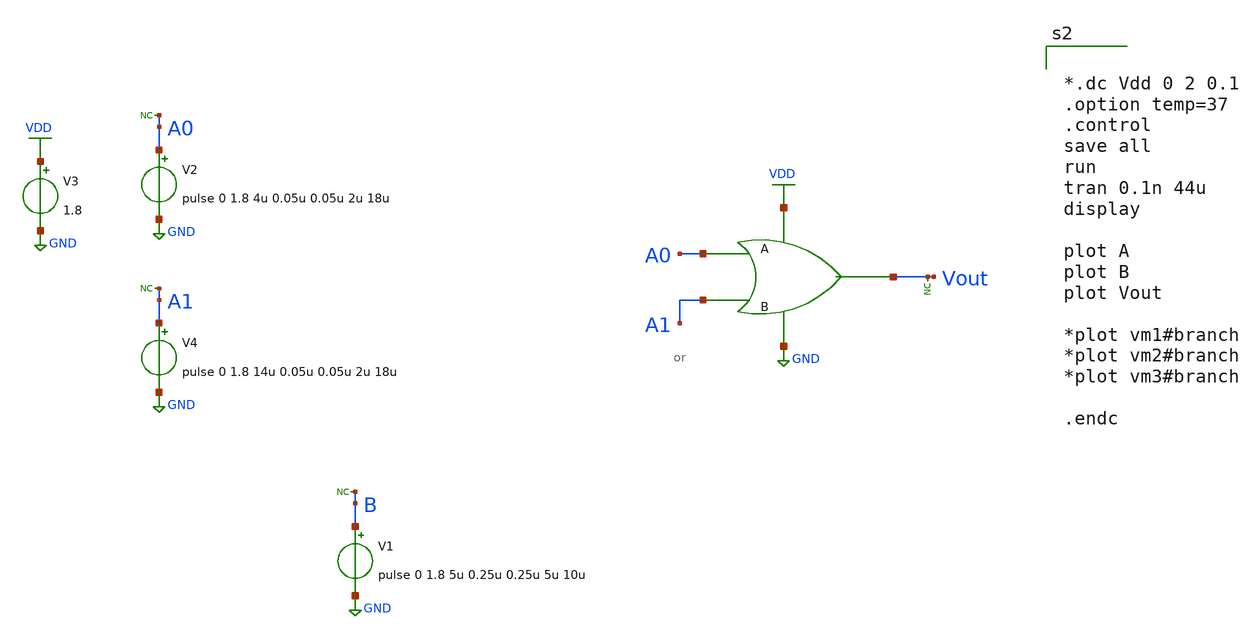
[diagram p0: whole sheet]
** sch_path: xschem/cmos_imager/row_select_clk.sch
**.subckt row_select_clk
V1 B GND pulse 0 1.8 5u 0.25u 0.25u 5u 10u
* noconn B
V2 A0 GND pulse 0 1.8 4u 0.05u 0.05u 2u 18u
* noconn A0
V3 VDD GND 1.8
X1 A0 Vout GND VDD A1 or
* noconn Vout
V4 A1 GND pulse 0 1.8 14u 0.05u 0.05u 2u 18u
* noconn A1
**** begin user architecture code

** opencircuitdesign pdks install
.lib $::SKYWATER_MODELS/sky130.lib.spice tt




*.dc Vdd 0 2 0.1
.option temp=37
.control
save all
run
tran 0.1n 44u
display

plot A
plot B
plot Vout

*plot vm1#branch
*plot vm2#branch
*plot vm3#branch

.endc


**** end user architecture code
**.ends
.GLOBAL GND
.GLOBAL VDD
.end
